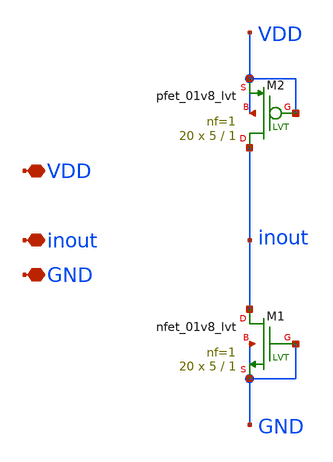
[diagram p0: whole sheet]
** sch_path: xschem/esd_half.sch
**.subckt esd_half VDD inout GND
*.iopin VDD
*.iopin inout
*.iopin GND
XM1 inout GND GND GND sky130_fd_pr__nfet_01v8_lvt L=1 W=5 nf=1 ad='int((nf+1)/2) * W/nf * 0.29' as='int((nf+2)/2) * W/nf * 0.29'
+ pd='2*int((nf+1)/2) * (W/nf + 0.29)' ps='2*int((nf+2)/2) * (W/nf + 0.29)' nrd='0.29 / W' nrs='0.29 / W'
+ sa=0 sb=0 sd=0 mult=20 m=20
XM2 inout VDD VDD VDD sky130_fd_pr__pfet_01v8_lvt L=1 W=5 nf=1 ad='int((nf+1)/2) * W/nf * 0.29' as='int((nf+2)/2) * W/nf * 0.29'
+ pd='2*int((nf+1)/2) * (W/nf + 0.29)' ps='2*int((nf+2)/2) * (W/nf + 0.29)' nrd='0.29 / W' nrs='0.29 / W'
+ sa=0 sb=0 sd=0 mult=20 m=20
**.ends
.end
